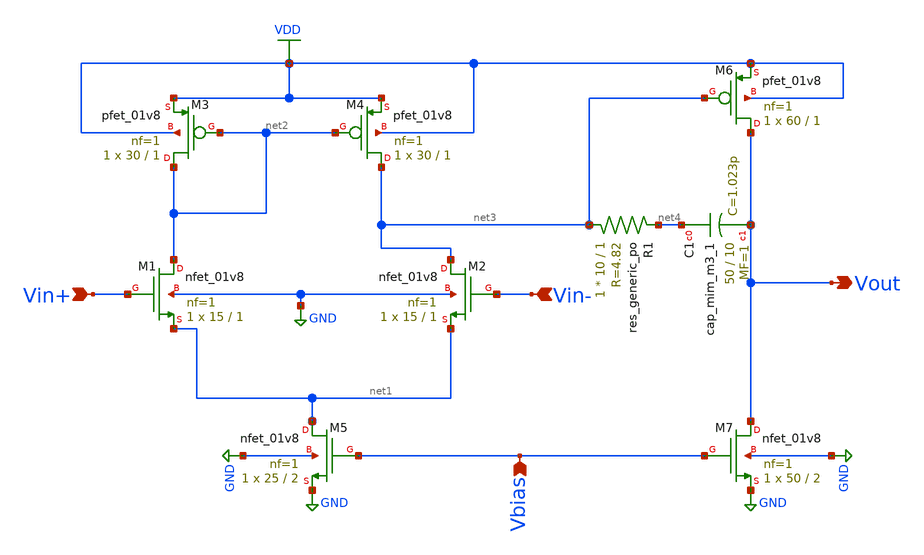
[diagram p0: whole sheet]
** sch_path: analog/schematics/bootcamp_opamp.sch
**.subckt bootcamp_opamp Vin+ Vbias Vin- Vout
*.ipin Vin+
*.ipin Vbias
*.ipin Vin-
*.opin Vout
XM1 net2 Vin+ net1 GND sky130_fd_pr__nfet_01v8 L=1 W=15 nf=1 ad='int((nf+1)/2) * W/nf * 0.29' as='int((nf+2)/2) * W/nf * 0.29'
+ pd='2*int((nf+1)/2) * (W/nf + 0.29)' ps='2*int((nf+2)/2) * (W/nf + 0.29)' nrd='0.29 / W' nrs='0.29 / W'
+ sa=0 sb=0 sd=0 mult=1 m=1
XM3 net2 net2 VDD VDD sky130_fd_pr__pfet_01v8 L=1 W=30 nf=1 ad='int((nf+1)/2) * W/nf * 0.29' as='int((nf+2)/2) * W/nf * 0.29'
+ pd='2*int((nf+1)/2) * (W/nf + 0.29)' ps='2*int((nf+2)/2) * (W/nf + 0.29)' nrd='0.29 / W' nrs='0.29 / W'
+ sa=0 sb=0 sd=0 mult=1 m=1
XM4 net3 net2 VDD VDD sky130_fd_pr__pfet_01v8 L=1 W=30 nf=1 ad='int((nf+1)/2) * W/nf * 0.29' as='int((nf+2)/2) * W/nf * 0.29'
+ pd='2*int((nf+1)/2) * (W/nf + 0.29)' ps='2*int((nf+2)/2) * (W/nf + 0.29)' nrd='0.29 / W' nrs='0.29 / W'
+ sa=0 sb=0 sd=0 mult=1 m=1
XM5 net1 Vbias GND GND sky130_fd_pr__nfet_01v8 L=2 W=25 nf=1 ad='int((nf+1)/2) * W/nf * 0.29' as='int((nf+2)/2) * W/nf * 0.29'
+ pd='2*int((nf+1)/2) * (W/nf + 0.29)' ps='2*int((nf+2)/2) * (W/nf + 0.29)' nrd='0.29 / W' nrs='0.29 / W'
+ sa=0 sb=0 sd=0 mult=1 m=1
XM2 net3 Vin- net1 GND sky130_fd_pr__nfet_01v8 L=1 W=15 nf=1 ad='int((nf+1)/2) * W/nf * 0.29' as='int((nf+2)/2) * W/nf * 0.29'
+ pd='2*int((nf+1)/2) * (W/nf + 0.29)' ps='2*int((nf+2)/2) * (W/nf + 0.29)' nrd='0.29 / W' nrs='0.29 / W'
+ sa=0 sb=0 sd=0 mult=1 m=1
XC1 net4 Vout sky130_fd_pr__cap_mim_m3_1 W=50 L=10 MF=1 m=1
XR1 net3 net4 sky130_fd_pr__res_generic_po W=10 L=1 m=1
XM7 Vout Vbias GND GND sky130_fd_pr__nfet_01v8 L=2 W=50 nf=1 ad='int((nf+1)/2) * W/nf * 0.29' as='int((nf+2)/2) * W/nf * 0.29'
+ pd='2*int((nf+1)/2) * (W/nf + 0.29)' ps='2*int((nf+2)/2) * (W/nf + 0.29)' nrd='0.29 / W' nrs='0.29 / W'
+ sa=0 sb=0 sd=0 mult=1 m=1
XM6 Vout net3 VDD VDD sky130_fd_pr__pfet_01v8 L=1 W=60 nf=1 ad='int((nf+1)/2) * W/nf * 0.29' as='int((nf+2)/2) * W/nf * 0.29'
+ pd='2*int((nf+1)/2) * (W/nf + 0.29)' ps='2*int((nf+2)/2) * (W/nf + 0.29)' nrd='0.29 / W' nrs='0.29 / W'
+ sa=0 sb=0 sd=0 mult=1 m=1
**.ends
.GLOBAL GND
.GLOBAL VDD
.end
